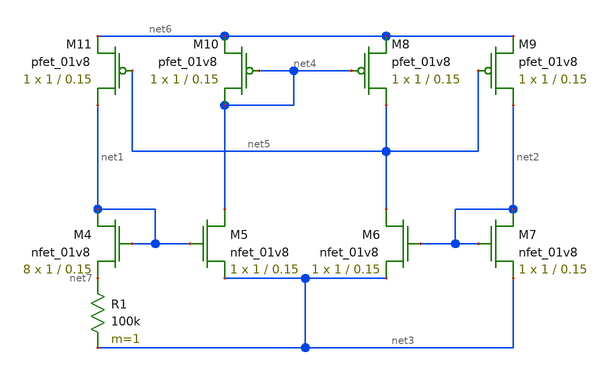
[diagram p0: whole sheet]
** sch_path: Miniproject3/Bias/current_bias.sch
**.subckt current_bias
XM4 net1 net1 net7 GND sky130_fd_pr__nfet_01v8 L=0.15 W=1 nf=1 ad='int((nf+1)/2) * W/nf * 0.29' as='int((nf+2)/2) * W/nf * 0.29'
+ pd='2*int((nf+1)/2) * (W/nf + 0.29)' ps='2*int((nf+2)/2) * (W/nf + 0.29)' nrd='0.29 / W' nrs='0.29 / W'
+ sa=0 sb=0 sd=0 mult=8 m=8
XM5 net4 net1 net3 GND sky130_fd_pr__nfet_01v8 L=0.15 W=1 nf=1 ad='int((nf+1)/2) * W/nf * 0.29' as='int((nf+2)/2) * W/nf * 0.29'
+ pd='2*int((nf+1)/2) * (W/nf + 0.29)' ps='2*int((nf+2)/2) * (W/nf + 0.29)' nrd='0.29 / W' nrs='0.29 / W'
+ sa=0 sb=0 sd=0 mult=1 m=1
XM6 net5 net2 net3 GND sky130_fd_pr__nfet_01v8 L=0.15 W=1 nf=1 ad='int((nf+1)/2) * W/nf * 0.29' as='int((nf+2)/2) * W/nf * 0.29'
+ pd='2*int((nf+1)/2) * (W/nf + 0.29)' ps='2*int((nf+2)/2) * (W/nf + 0.29)' nrd='0.29 / W' nrs='0.29 / W'
+ sa=0 sb=0 sd=0 mult=1 m=1
XM7 net2 net2 net3 GND sky130_fd_pr__nfet_01v8 L=0.15 W=1 nf=1 ad='int((nf+1)/2) * W/nf * 0.29' as='int((nf+2)/2) * W/nf * 0.29'
+ pd='2*int((nf+1)/2) * (W/nf + 0.29)' ps='2*int((nf+2)/2) * (W/nf + 0.29)' nrd='0.29 / W' nrs='0.29 / W'
+ sa=0 sb=0 sd=0 mult=1 m=1
R1 net7 net3 100k m=1
XM8 net5 net4 net6 VDD sky130_fd_pr__pfet_01v8 L=0.15 W=1 nf=1 ad='int((nf+1)/2) * W/nf * 0.29' as='int((nf+2)/2) * W/nf * 0.29'
+ pd='2*int((nf+1)/2) * (W/nf + 0.29)' ps='2*int((nf+2)/2) * (W/nf + 0.29)' nrd='0.29 / W' nrs='0.29 / W'
+ sa=0 sb=0 sd=0 mult=1 m=1
XM9 net2 net5 net6 VDD sky130_fd_pr__pfet_01v8 L=0.15 W=1 nf=1 ad='int((nf+1)/2) * W/nf * 0.29' as='int((nf+2)/2) * W/nf * 0.29'
+ pd='2*int((nf+1)/2) * (W/nf + 0.29)' ps='2*int((nf+2)/2) * (W/nf + 0.29)' nrd='0.29 / W' nrs='0.29 / W'
+ sa=0 sb=0 sd=0 mult=1 m=1
XM10 net4 net4 net6 VDD sky130_fd_pr__pfet_01v8 L=0.15 W=1 nf=1 ad='int((nf+1)/2) * W/nf * 0.29' as='int((nf+2)/2) * W/nf * 0.29'
+ pd='2*int((nf+1)/2) * (W/nf + 0.29)' ps='2*int((nf+2)/2) * (W/nf + 0.29)' nrd='0.29 / W' nrs='0.29 / W'
+ sa=0 sb=0 sd=0 mult=1 m=1
XM11 net1 net5 net6 VDD sky130_fd_pr__pfet_01v8 L=0.15 W=1 nf=1 ad='int((nf+1)/2) * W/nf * 0.29' as='int((nf+2)/2) * W/nf * 0.29'
+ pd='2*int((nf+1)/2) * (W/nf + 0.29)' ps='2*int((nf+2)/2) * (W/nf + 0.29)' nrd='0.29 / W' nrs='0.29 / W'
+ sa=0 sb=0 sd=0 mult=1 m=1
**.ends
.end
